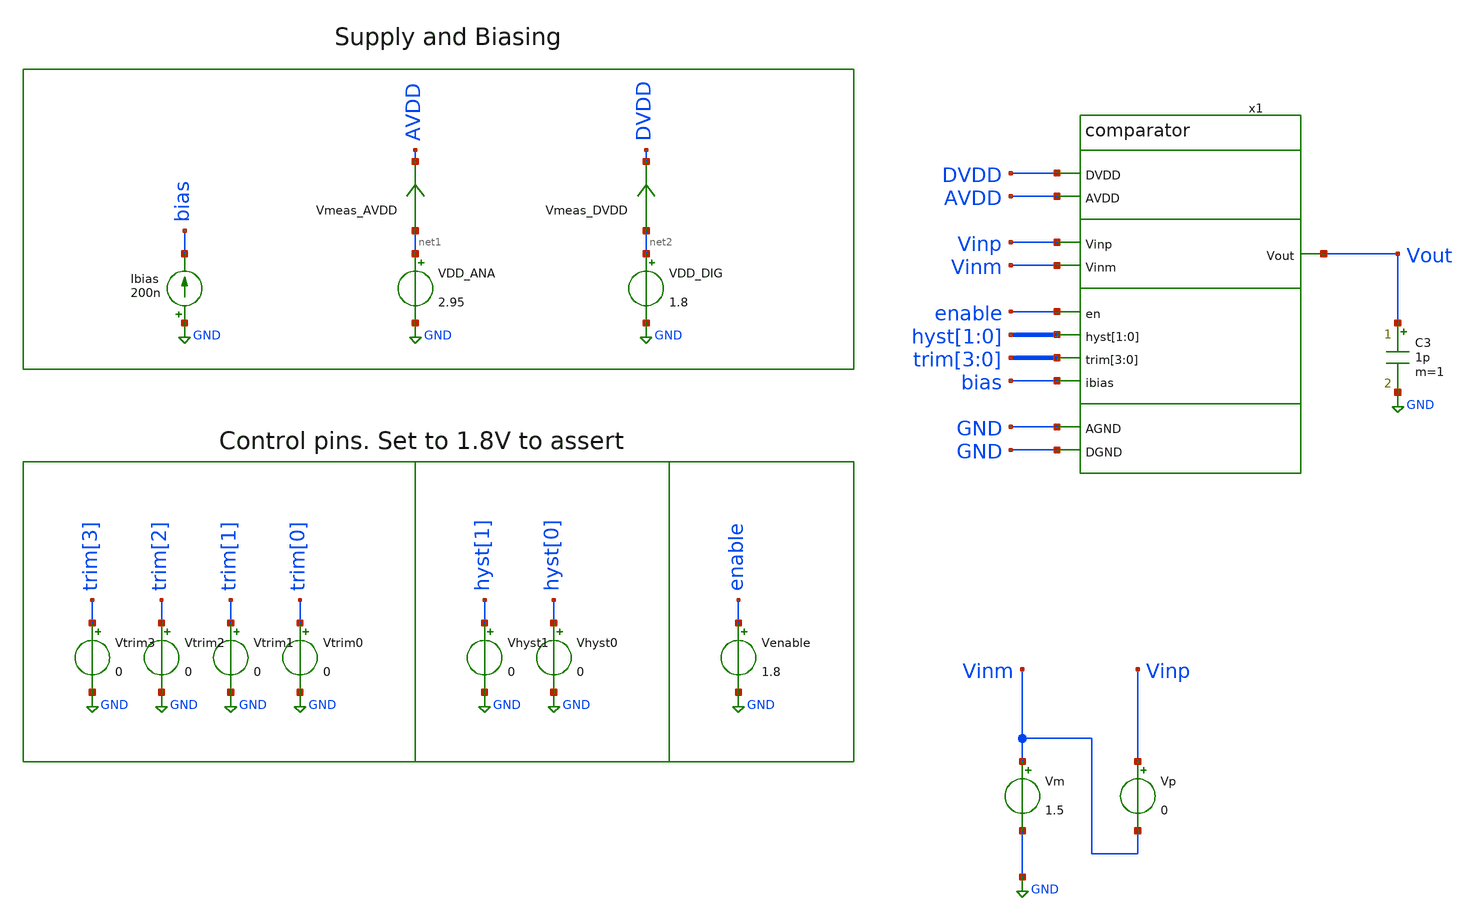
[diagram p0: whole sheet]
** sch_path: xschem/tb_comparator.sch
**.subckt tb_comparator
Vtrim3 trim[3] GND 0
Vp Vinp Vinm 0
VDD_ANA net1 GND 2.95
VDD_DIG net2 GND 1.8
Ibias GND bias 200n
C3 Vout GND 1p m=1
Vtrim2 trim[2] GND 0
Vtrim1 trim[1] GND 0
Vtrim0 trim[0] GND 0
Vm Vinm GND 1.5
Vhyst1 hyst[1] GND 0
Vhyst0 hyst[0] GND 0
x1 DVDD AVDD GND GND Vinp Vout Vinm enable hyst[1] hyst[0] trim[3] trim[2] trim[1] trim[0] bias
+ comparator
Venable enable GND 1.8
Vmeas_AVDD net1 AVDD 0
.save i(vmeas_avdd)
Vmeas_DVDD net2 DVDD 0
.save i(vmeas_dvdd)
**** begin user architecture code
.lib $::SKYWATER_MODELS/sky130.lib.spice tt



   *.dc Vp -10m 10m 0.05m Vm 0 5 0.25
   *.dc Vm 0 5 0.05 Vp -100m 100m 10m
   *.dc Vp 0 5 0.01
   .tran 100n 1m
.control
   *.tran 10n 13u 9u
   plot v(Vout)
   *plot v(Vinp)
   *plot v(Vinm)
   *plot v(x1.cmfb)
   *plot v(x1.vop)
   *plot v(x1.vom)
   *plot (v(x1.vop)+v(x1.vom))/2
   *plot v(x1.vop)-v(x1.vom)
   *plot v(x1.vdiff)
   meas tran current_avdd avg i(vmeas_avdd) from=500u to=1m
   meas tran current_dvdd avg i(vmeas_dvdd) from=500u to=1m
   wrdata test.txt current_avdd
.endc
.save all


**** end user architecture code
**.ends

* expanding   symbol:  comparator.sym # of pins=11
** sym_path: xschem/comparator.sym
** sch_path: xschem/comparator.sch
.subckt comparator DVDD AVDD AGND DGND Vinp Vout Vinm en hyst[1] hyst[0] trim[3] trim[2] trim[1]
+ trim[0] ibias
*.ipin Vinp
*.ipin Vinm
*.ipin AVDD
*.ipin AGND
*.ipin en
*.ipin hyst[1],hyst[0]
*.ipin trim[3],trim[2],trim[1],trim[0]
*.opin Vout
*.ipin DVDD
*.ipin ibias
*.ipin DGND
XM7 bias_n bias_n AGND AGND sky130_fd_pr__nfet_g5v0d10v5 L=1 W=2 nf=1 ad='int((nf+1)/2) * W/nf * 0.29'
+ as='int((nf+2)/2) * W/nf * 0.29' pd='2*int((nf+1)/2) * (W/nf + 0.29)' ps='2*int((nf+2)/2) * (W/nf + 0.29)'
+ nrd='0.29 / W' nrs='0.29 / W' sa=0 sb=0 sd=0 mult=2 m=2
XM6 stg1m_bot Vinm Vxm AGND sky130_fd_pr__nfet_g5v0d10v5 L=1 W=2 nf=1 ad='int((nf+1)/2) * W/nf * 0.29'
+ as='int((nf+2)/2) * W/nf * 0.29' pd='2*int((nf+1)/2) * (W/nf + 0.29)' ps='2*int((nf+2)/2) * (W/nf + 0.29)'
+ nrd='0.29 / W' nrs='0.29 / W' sa=0 sb=0 sd=0 mult=10 m=10
XM2 net1 bias_n AGND AGND sky130_fd_pr__nfet_g5v0d10v5 L=1 W=2 nf=1 ad='int((nf+1)/2) * W/nf * 0.29'
+ as='int((nf+2)/2) * W/nf * 0.29' pd='2*int((nf+1)/2) * (W/nf + 0.29)' ps='2*int((nf+2)/2) * (W/nf + 0.29)'
+ nrd='0.29 / W' nrs='0.29 / W' sa=0 sb=0 sd=0 mult=4 m=4
XM1 stg1p_bot Vinp Vxm AGND sky130_fd_pr__nfet_g5v0d10v5 L=1 W=2 nf=1 ad='int((nf+1)/2) * W/nf * 0.29'
+ as='int((nf+2)/2) * W/nf * 0.29' pd='2*int((nf+1)/2) * (W/nf + 0.29)' ps='2*int((nf+2)/2) * (W/nf + 0.29)'
+ nrd='0.29 / W' nrs='0.29 / W' sa=0 sb=0 sd=0 mult=10 m=10
XM3 stg1m_top stg1m_top AGND AGND sky130_fd_pr__nfet_g5v0d10v5 L=1 W=2 nf=1 ad='int((nf+1)/2) * W/nf * 0.29'
+ as='int((nf+2)/2) * W/nf * 0.29' pd='2*int((nf+1)/2) * (W/nf + 0.29)' ps='2*int((nf+2)/2) * (W/nf + 0.29)'
+ nrd='0.29 / W' nrs='0.29 / W' sa=0 sb=0 sd=0 mult=2 m=2
XM4 net7 bias_var AVDD AVDD sky130_fd_pr__pfet_g5v0d10v5 L=1 W=4 nf=2 ad='int((nf+1)/2) * W/nf * 0.29'
+ as='int((nf+2)/2) * W/nf * 0.29' pd='2*int((nf+1)/2) * (W/nf + 0.29)' ps='2*int((nf+2)/2) * (W/nf + 0.29)'
+ nrd='0.29 / W' nrs='0.29 / W' sa=0 sb=0 sd=0 mult=4 m=4
XM5 stg1m_top Vinm Vxp AVDD sky130_fd_pr__pfet_g5v0d10v5 L=1 W=4 nf=2 ad='int((nf+1)/2) * W/nf * 0.29'
+ as='int((nf+2)/2) * W/nf * 0.29' pd='2*int((nf+1)/2) * (W/nf + 0.29)' ps='2*int((nf+2)/2) * (W/nf + 0.29)'
+ nrd='0.29 / W' nrs='0.29 / W' sa=0 sb=0 sd=0 mult=10 m=10
XM17 stg1p_top Vinp Vxp AVDD sky130_fd_pr__pfet_g5v0d10v5 L=1 W=4 nf=2 ad='int((nf+1)/2) * W/nf * 0.29'
+ as='int((nf+2)/2) * W/nf * 0.29' pd='2*int((nf+1)/2) * (W/nf + 0.29)' ps='2*int((nf+2)/2) * (W/nf + 0.29)'
+ nrd='0.29 / W' nrs='0.29 / W' sa=0 sb=0 sd=0 mult=10 m=10
XM13 stg1m_bot stg1m_bot AVDD AVDD sky130_fd_pr__pfet_g5v0d10v5 L=1 W=4 nf=2 ad='int((nf+1)/2) * W/nf * 0.29'
+ as='int((nf+2)/2) * W/nf * 0.29' pd='2*int((nf+1)/2) * (W/nf + 0.29)' ps='2*int((nf+2)/2) * (W/nf + 0.29)'
+ nrd='0.29 / W' nrs='0.29 / W' sa=0 sb=0 sd=0 mult=2 m=2
XM9 Vop stg1m_bot AVDD AVDD sky130_fd_pr__pfet_g5v0d10v5 L=1 W=4 nf=2 ad='int((nf+1)/2) * W/nf * 0.29'
+ as='int((nf+2)/2) * W/nf * 0.29' pd='2*int((nf+1)/2) * (W/nf + 0.29)' ps='2*int((nf+2)/2) * (W/nf + 0.29)'
+ nrd='0.29 / W' nrs='0.29 / W' sa=0 sb=0 sd=0 mult=4 m=4
XM10 Vop stg1m_top AGND AGND sky130_fd_pr__nfet_g5v0d10v5 L=1 W=2 nf=1 ad='int((nf+1)/2) * W/nf * 0.29'
+ as='int((nf+2)/2) * W/nf * 0.29' pd='2*int((nf+1)/2) * (W/nf + 0.29)' ps='2*int((nf+2)/2) * (W/nf + 0.29)'
+ nrd='0.29 / W' nrs='0.29 / W' sa=0 sb=0 sd=0 mult=4 m=4
XM8 Vom stg1p_top AGND AGND sky130_fd_pr__nfet_g5v0d10v5 L=1 W=2 nf=1 ad='int((nf+1)/2) * W/nf * 0.29'
+ as='int((nf+2)/2) * W/nf * 0.29' pd='2*int((nf+1)/2) * (W/nf + 0.29)' ps='2*int((nf+2)/2) * (W/nf + 0.29)'
+ nrd='0.29 / W' nrs='0.29 / W' sa=0 sb=0 sd=0 mult=4 m=4
XM11 stg1p_top stg1p_top AGND AGND sky130_fd_pr__nfet_g5v0d10v5 L=1 W=2 nf=1 ad='int((nf+1)/2) * W/nf * 0.29'
+ as='int((nf+2)/2) * W/nf * 0.29' pd='2*int((nf+1)/2) * (W/nf + 0.29)' ps='2*int((nf+2)/2) * (W/nf + 0.29)'
+ nrd='0.29 / W' nrs='0.29 / W' sa=0 sb=0 sd=0 mult=2 m=2
XM12 Vom stg1p_bot AVDD AVDD sky130_fd_pr__pfet_g5v0d10v5 L=1 W=4 nf=2 ad='int((nf+1)/2) * W/nf * 0.29'
+ as='int((nf+2)/2) * W/nf * 0.29' pd='2*int((nf+1)/2) * (W/nf + 0.29)' ps='2*int((nf+2)/2) * (W/nf + 0.29)'
+ nrd='0.29 / W' nrs='0.29 / W' sa=0 sb=0 sd=0 mult=4 m=4
XM14 stg1p_bot stg1p_bot AVDD AVDD sky130_fd_pr__pfet_g5v0d10v5 L=1 W=4 nf=2 ad='int((nf+1)/2) * W/nf * 0.29'
+ as='int((nf+2)/2) * W/nf * 0.29' pd='2*int((nf+1)/2) * (W/nf + 0.29)' ps='2*int((nf+2)/2) * (W/nf + 0.29)'
+ nrd='0.29 / W' nrs='0.29 / W' sa=0 sb=0 sd=0 mult=2 m=2
XM18 Vom cmfb AGND AGND sky130_fd_pr__nfet_g5v0d10v5 L=1 W=2 nf=1 ad='int((nf+1)/2) * W/nf * 0.29' as='int((nf+2)/2) * W/nf * 0.29'
+ pd='2*int((nf+1)/2) * (W/nf + 0.29)' ps='2*int((nf+2)/2) * (W/nf + 0.29)' nrd='0.29 / W' nrs='0.29 / W'
+ sa=0 sb=0 sd=0 mult=4 m=4
XM19 Vop cmfb AGND AGND sky130_fd_pr__nfet_g5v0d10v5 L=1 W=2 nf=1 ad='int((nf+1)/2) * W/nf * 0.29' as='int((nf+2)/2) * W/nf * 0.29'
+ pd='2*int((nf+1)/2) * (W/nf + 0.29)' ps='2*int((nf+2)/2) * (W/nf + 0.29)' nrd='0.29 / W' nrs='0.29 / W'
+ sa=0 sb=0 sd=0 mult=4 m=4
XM20 Vom bias_var AVDD AVDD sky130_fd_pr__pfet_g5v0d10v5 L=1 W=4 nf=2 ad='int((nf+1)/2) * W/nf * 0.29'
+ as='int((nf+2)/2) * W/nf * 0.29' pd='2*int((nf+1)/2) * (W/nf + 0.29)' ps='2*int((nf+2)/2) * (W/nf + 0.29)'
+ nrd='0.29 / W' nrs='0.29 / W' sa=0 sb=0 sd=0 mult=6 m=6
XM21 Vop bias_var AVDD AVDD sky130_fd_pr__pfet_g5v0d10v5 L=1 W=4 nf=2 ad='int((nf+1)/2) * W/nf * 0.29'
+ as='int((nf+2)/2) * W/nf * 0.29' pd='2*int((nf+1)/2) * (W/nf + 0.29)' ps='2*int((nf+2)/2) * (W/nf + 0.29)'
+ nrd='0.29 / W' nrs='0.29 / W' sa=0 sb=0 sd=0 mult=6 m=6
XM22 net2 bias_p AVDD AVDD sky130_fd_pr__pfet_g5v0d10v5 L=1 W=4 nf=2 ad='int((nf+1)/2) * W/nf * 0.29'
+ as='int((nf+2)/2) * W/nf * 0.29' pd='2*int((nf+1)/2) * (W/nf + 0.29)' ps='2*int((nf+2)/2) * (W/nf + 0.29)'
+ nrd='0.29 / W' nrs='0.29 / W' sa=0 sb=0 sd=0 mult=2 m=2
XM23 Vom_stg2 Vom net2 AVDD sky130_fd_pr__pfet_g5v0d10v5 L=1 W=4 nf=2 ad='int((nf+1)/2) * W/nf * 0.29'
+ as='int((nf+2)/2) * W/nf * 0.29' pd='2*int((nf+1)/2) * (W/nf + 0.29)' ps='2*int((nf+2)/2) * (W/nf + 0.29)'
+ nrd='0.29 / W' nrs='0.29 / W' sa=0 sb=0 sd=0 mult=2 m=2
XM24 Vop_stg2 Vop net2 AVDD sky130_fd_pr__pfet_g5v0d10v5 L=1 W=4 nf=2 ad='int((nf+1)/2) * W/nf * 0.29'
+ as='int((nf+2)/2) * W/nf * 0.29' pd='2*int((nf+1)/2) * (W/nf + 0.29)' ps='2*int((nf+2)/2) * (W/nf + 0.29)'
+ nrd='0.29 / W' nrs='0.29 / W' sa=0 sb=0 sd=0 mult=2 m=2
XM25 Vop_stg2 Vop_stg2 DGND DGND sky130_fd_pr__nfet_g5v0d10v5 L=1 W=2 nf=1 ad='int((nf+1)/2) * W/nf * 0.29'
+ as='int((nf+2)/2) * W/nf * 0.29' pd='2*int((nf+1)/2) * (W/nf + 0.29)' ps='2*int((nf+2)/2) * (W/nf + 0.29)'
+ nrd='0.29 / W' nrs='0.29 / W' sa=0 sb=0 sd=0 mult=2 m=2
XM26 Vom_stg2 Vom_stg2 DGND DGND sky130_fd_pr__nfet_g5v0d10v5 L=1 W=2 nf=1 ad='int((nf+1)/2) * W/nf * 0.29'
+ as='int((nf+2)/2) * W/nf * 0.29' pd='2*int((nf+1)/2) * (W/nf + 0.29)' ps='2*int((nf+2)/2) * (W/nf + 0.29)'
+ nrd='0.29 / W' nrs='0.29 / W' sa=0 sb=0 sd=0 mult=2 m=2
XM27 net3 Vom_stg2 DGND DGND sky130_fd_pr__nfet_g5v0d10v5 L=1 W=2 nf=1 ad='int((nf+1)/2) * W/nf * 0.29'
+ as='int((nf+2)/2) * W/nf * 0.29' pd='2*int((nf+1)/2) * (W/nf + 0.29)' ps='2*int((nf+2)/2) * (W/nf + 0.29)'
+ nrd='0.29 / W' nrs='0.29 / W' sa=0 sb=0 sd=0 mult=2 m=2
XM28 Vdiff Vop_stg2 DGND DGND sky130_fd_pr__nfet_g5v0d10v5 L=1 W=2 nf=1 ad='int((nf+1)/2) * W/nf * 0.29'
+ as='int((nf+2)/2) * W/nf * 0.29' pd='2*int((nf+1)/2) * (W/nf + 0.29)' ps='2*int((nf+2)/2) * (W/nf + 0.29)'
+ nrd='0.29 / W' nrs='0.29 / W' sa=0 sb=0 sd=0 mult=2 m=2
XM29 Vdiff net3 DVDD DVDD sky130_fd_pr__pfet_01v8 L=1 W=4 nf=1 ad='int((nf+1)/2) * W/nf * 0.29' as='int((nf+2)/2) * W/nf * 0.29'
+ pd='2*int((nf+1)/2) * (W/nf + 0.29)' ps='2*int((nf+2)/2) * (W/nf + 0.29)' nrd='0.29 / W' nrs='0.29 / W'
+ sa=0 sb=0 sd=0 mult=2 m=2
XM30 net3 net3 DVDD DVDD sky130_fd_pr__pfet_01v8 L=1 W=4 nf=1 ad='int((nf+1)/2) * W/nf * 0.29' as='int((nf+2)/2) * W/nf * 0.29'
+ pd='2*int((nf+1)/2) * (W/nf + 0.29)' ps='2*int((nf+2)/2) * (W/nf + 0.29)' nrd='0.29 / W' nrs='0.29 / W'
+ sa=0 sb=0 sd=0 mult=2 m=2
XM31 Vout Vdiff DVDD DVDD sky130_fd_pr__pfet_01v8 L=0.15 W=1 nf=2 ad='int((nf+1)/2) * W/nf * 0.29' as='int((nf+2)/2) * W/nf * 0.29'
+ pd='2*int((nf+1)/2) * (W/nf + 0.29)' ps='2*int((nf+2)/2) * (W/nf + 0.29)' nrd='0.29 / W' nrs='0.29 / W'
+ sa=0 sb=0 sd=0 mult=1 m=1
XM44 Vout Vdiff DGND DGND sky130_fd_pr__nfet_01v8 L=0.15 W=0.5 nf=1 ad='int((nf+1)/2) * W/nf * 0.29'
+ as='int((nf+2)/2) * W/nf * 0.29' pd='2*int((nf+1)/2) * (W/nf + 0.29)' ps='2*int((nf+2)/2) * (W/nf + 0.29)'
+ nrd='0.29 / W' nrs='0.29 / W' sa=0 sb=0 sd=0 mult=1 m=1
XM45 ibias ibias bias_n AGND sky130_fd_pr__nfet_g5v0d10v5 L=1 W=2 nf=1 ad='int((nf+1)/2) * W/nf * 0.29'
+ as='int((nf+2)/2) * W/nf * 0.29' pd='2*int((nf+1)/2) * (W/nf + 0.29)' ps='2*int((nf+2)/2) * (W/nf + 0.29)'
+ nrd='0.29 / W' nrs='0.29 / W' sa=0 sb=0 sd=0 mult=1 m=1
XM48 bias_n enb_hv AGND AGND sky130_fd_pr__nfet_g5v0d10v5 L=0.5 W=2 nf=1 ad='int((nf+1)/2) * W/nf * 0.29'
+ as='int((nf+2)/2) * W/nf * 0.29' pd='2*int((nf+1)/2) * (W/nf + 0.29)' ps='2*int((nf+2)/2) * (W/nf + 0.29)'
+ nrd='0.29 / W' nrs='0.29 / W' sa=0 sb=0 sd=0 mult=4 m=4
XM40 net4 bias_hyst net8 AGND sky130_fd_pr__nfet_g5v0d10v5 L=1 W=2 nf=1 ad='int((nf+1)/2) * W/nf * 0.29'
+ as='int((nf+2)/2) * W/nf * 0.29' pd='2*int((nf+1)/2) * (W/nf + 0.29)' ps='2*int((nf+2)/2) * (W/nf + 0.29)'
+ nrd='0.29 / W' nrs='0.29 / W' sa=0 sb=0 sd=0 mult=3 m=3
XM53 net11 Vout net4 AGND sky130_fd_pr__nfet_g5v0d10v5 L=1 W=2 nf=1 ad='int((nf+1)/2) * W/nf * 0.29'
+ as='int((nf+2)/2) * W/nf * 0.29' pd='2*int((nf+1)/2) * (W/nf + 0.29)' ps='2*int((nf+2)/2) * (W/nf + 0.29)'
+ nrd='0.29 / W' nrs='0.29 / W' sa=0 sb=0 sd=0 mult=1 m=1
XM54 net10 Voutb net4 AGND sky130_fd_pr__nfet_g5v0d10v5 L=1 W=2 nf=1 ad='int((nf+1)/2) * W/nf * 0.29'
+ as='int((nf+2)/2) * W/nf * 0.29' pd='2*int((nf+1)/2) * (W/nf + 0.29)' ps='2*int((nf+2)/2) * (W/nf + 0.29)'
+ nrd='0.29 / W' nrs='0.29 / W' sa=0 sb=0 sd=0 mult=1 m=1
XM61 net5 stg1p_bot AVDD AVDD sky130_fd_pr__pfet_g5v0d10v5 L=1 W=4 nf=2 ad='int((nf+1)/2) * W/nf * 0.29'
+ as='int((nf+2)/2) * W/nf * 0.29' pd='2*int((nf+1)/2) * (W/nf + 0.29)' ps='2*int((nf+2)/2) * (W/nf + 0.29)'
+ nrd='0.29 / W' nrs='0.29 / W' sa=0 sb=0 sd=0 mult=2 m=2
XM62 net5 stg1m_bot AVDD AVDD sky130_fd_pr__pfet_g5v0d10v5 L=1 W=4 nf=2 ad='int((nf+1)/2) * W/nf * 0.29'
+ as='int((nf+2)/2) * W/nf * 0.29' pd='2*int((nf+1)/2) * (W/nf + 0.29)' ps='2*int((nf+2)/2) * (W/nf + 0.29)'
+ nrd='0.29 / W' nrs='0.29 / W' sa=0 sb=0 sd=0 mult=2 m=2
XM70 net5 bias_n AGND AGND sky130_fd_pr__nfet_g5v0d10v5 L=1 W=2 nf=1 ad='int((nf+1)/2) * W/nf * 0.29'
+ as='int((nf+2)/2) * W/nf * 0.29' pd='2*int((nf+1)/2) * (W/nf + 0.29)' ps='2*int((nf+2)/2) * (W/nf + 0.29)'
+ nrd='0.29 / W' nrs='0.29 / W' sa=0 sb=0 sd=0 mult=4 m=4
XM72 bias_var bias_var AVDD AVDD sky130_fd_pr__pfet_g5v0d10v5 L=1 W=4 nf=2 ad='int((nf+1)/2) * W/nf * 0.29'
+ as='int((nf+2)/2) * W/nf * 0.29' pd='2*int((nf+1)/2) * (W/nf + 0.29)' ps='2*int((nf+2)/2) * (W/nf + 0.29)'
+ nrd='0.29 / W' nrs='0.29 / W' sa=0 sb=0 sd=0 mult=4 m=4
XM63 net5 net5 bias_var AVDD sky130_fd_pr__pfet_g5v0d10v5 L=1 W=4 nf=2 ad='int((nf+1)/2) * W/nf * 0.29'
+ as='int((nf+2)/2) * W/nf * 0.29' pd='2*int((nf+1)/2) * (W/nf + 0.29)' ps='2*int((nf+2)/2) * (W/nf + 0.29)'
+ nrd='0.29 / W' nrs='0.29 / W' sa=0 sb=0 sd=0 mult=4 m=4
XM64 Vom bias_p AVDD AVDD sky130_fd_pr__pfet_g5v0d10v5 L=1 W=4 nf=2 ad='int((nf+1)/2) * W/nf * 0.29'
+ as='int((nf+2)/2) * W/nf * 0.29' pd='2*int((nf+1)/2) * (W/nf + 0.29)' ps='2*int((nf+2)/2) * (W/nf + 0.29)'
+ nrd='0.29 / W' nrs='0.29 / W' sa=0 sb=0 sd=0 mult=2 m=2
XM71 Vop bias_p AVDD AVDD sky130_fd_pr__pfet_g5v0d10v5 L=1 W=4 nf=2 ad='int((nf+1)/2) * W/nf * 0.29'
+ as='int((nf+2)/2) * W/nf * 0.29' pd='2*int((nf+1)/2) * (W/nf + 0.29)' ps='2*int((nf+2)/2) * (W/nf + 0.29)'
+ nrd='0.29 / W' nrs='0.29 / W' sa=0 sb=0 sd=0 mult=2 m=2
XM73 net4 bias_hyst net9 AGND sky130_fd_pr__nfet_g5v0d10v5 L=1 W=2 nf=1 ad='int((nf+1)/2) * W/nf * 0.29'
+ as='int((nf+2)/2) * W/nf * 0.29' pd='2*int((nf+1)/2) * (W/nf + 0.29)' ps='2*int((nf+2)/2) * (W/nf + 0.29)'
+ nrd='0.29 / W' nrs='0.29 / W' sa=0 sb=0 sd=0 mult=1 m=1
XM75 Voutb Vout DVDD DVDD sky130_fd_pr__pfet_01v8 L=0.15 W=1 nf=2 ad='int((nf+1)/2) * W/nf * 0.29' as='int((nf+2)/2) * W/nf * 0.29'
+ pd='2*int((nf+1)/2) * (W/nf + 0.29)' ps='2*int((nf+2)/2) * (W/nf + 0.29)' nrd='0.29 / W' nrs='0.29 / W'
+ sa=0 sb=0 sd=0 mult=1 m=1
XM76 Voutb Vout DGND DGND sky130_fd_pr__nfet_01v8 L=0.15 W=0.5 nf=1 ad='int((nf+1)/2) * W/nf * 0.29'
+ as='int((nf+2)/2) * W/nf * 0.29' pd='2*int((nf+1)/2) * (W/nf + 0.29)' ps='2*int((nf+2)/2) * (W/nf + 0.29)'
+ nrd='0.29 / W' nrs='0.29 / W' sa=0 sb=0 sd=0 mult=1 m=1
XM77 bias_p2 bias_p AVDD AVDD sky130_fd_pr__pfet_g5v0d10v5 L=1 W=4 nf=2 ad='int((nf+1)/2) * W/nf * 0.29'
+ as='int((nf+2)/2) * W/nf * 0.29' pd='2*int((nf+1)/2) * (W/nf + 0.29)' ps='2*int((nf+2)/2) * (W/nf + 0.29)'
+ nrd='0.29 / W' nrs='0.29 / W' sa=0 sb=0 sd=0 mult=2 m=2
XM78 bias_hyst bias_hyst AGND AGND sky130_fd_pr__nfet_g5v0d10v5 L=1 W=2 nf=1 ad='int((nf+1)/2) * W/nf * 0.29'
+ as='int((nf+2)/2) * W/nf * 0.29' pd='2*int((nf+1)/2) * (W/nf + 0.29)' ps='2*int((nf+2)/2) * (W/nf + 0.29)'
+ nrd='0.29 / W' nrs='0.29 / W' sa=0 sb=0 sd=0 mult=6 m=6
XM79 bias_hyst net6 bias_p2 AVDD sky130_fd_pr__pfet_g5v0d10v5 L=1 W=4 nf=2 ad='int((nf+1)/2) * W/nf * 0.29'
+ as='int((nf+2)/2) * W/nf * 0.29' pd='2*int((nf+1)/2) * (W/nf + 0.29)' ps='2*int((nf+2)/2) * (W/nf + 0.29)'
+ nrd='0.29 / W' nrs='0.29 / W' sa=0 sb=0 sd=0 mult=8 m=8
XM90 Vxm ibias net1 AGND sky130_fd_pr__nfet_g5v0d10v5 L=1 W=2 nf=1 ad='int((nf+1)/2) * W/nf * 0.29' as='int((nf+2)/2) * W/nf * 0.29'
+ pd='2*int((nf+1)/2) * (W/nf + 0.29)' ps='2*int((nf+2)/2) * (W/nf + 0.29)' nrd='0.29 / W' nrs='0.29 / W'
+ sa=0 sb=0 sd=0 mult=4 m=4
XM91 Vxp bias_p2 net7 AVDD sky130_fd_pr__pfet_g5v0d10v5 L=1 W=4 nf=2 ad='int((nf+1)/2) * W/nf * 0.29'
+ as='int((nf+2)/2) * W/nf * 0.29' pd='2*int((nf+1)/2) * (W/nf + 0.29)' ps='2*int((nf+2)/2) * (W/nf + 0.29)'
+ nrd='0.29 / W' nrs='0.29 / W' sa=0 sb=0 sd=0 mult=4 m=4
XM94 net6 bias_n AGND AGND sky130_fd_pr__nfet_g5v0d10v5 L=1 W=2 nf=1 ad='int((nf+1)/2) * W/nf * 0.29'
+ as='int((nf+2)/2) * W/nf * 0.29' pd='2*int((nf+1)/2) * (W/nf + 0.29)' ps='2*int((nf+2)/2) * (W/nf + 0.29)'
+ nrd='0.29 / W' nrs='0.29 / W' sa=0 sb=0 sd=0 mult=2 m=2
XM95 bias_p bias_p AVDD AVDD sky130_fd_pr__pfet_g5v0d10v5 L=1 W=4 nf=2 ad='int((nf+1)/2) * W/nf * 0.29'
+ as='int((nf+2)/2) * W/nf * 0.29' pd='2*int((nf+1)/2) * (W/nf + 0.29)' ps='2*int((nf+2)/2) * (W/nf + 0.29)'
+ nrd='0.29 / W' nrs='0.29 / W' sa=0 sb=0 sd=0 mult=2 m=2
XM96 net6 net6 bias_p AVDD sky130_fd_pr__pfet_g5v0d10v5 L=1 W=4 nf=2 ad='int((nf+1)/2) * W/nf * 0.29'
+ as='int((nf+2)/2) * W/nf * 0.29' pd='2*int((nf+1)/2) * (W/nf + 0.29)' ps='2*int((nf+2)/2) * (W/nf + 0.29)'
+ nrd='0.29 / W' nrs='0.29 / W' sa=0 sb=0 sd=0 mult=1 m=1
XM16 net8 hyst1_hv AGND AGND sky130_fd_pr__nfet_g5v0d10v5 L=0.5 W=2 nf=1 ad='int((nf+1)/2) * W/nf * 0.29'
+ as='int((nf+2)/2) * W/nf * 0.29' pd='2*int((nf+1)/2) * (W/nf + 0.29)' ps='2*int((nf+2)/2) * (W/nf + 0.29)'
+ nrd='0.29 / W' nrs='0.29 / W' sa=0 sb=0 sd=0 mult=6 m=6
XM33 net9 hyst0_hv AGND AGND sky130_fd_pr__nfet_g5v0d10v5 L=0.5 W=2 nf=1 ad='int((nf+1)/2) * W/nf * 0.29'
+ as='int((nf+2)/2) * W/nf * 0.29' pd='2*int((nf+1)/2) * (W/nf + 0.29)' ps='2*int((nf+2)/2) * (W/nf + 0.29)'
+ nrd='0.29 / W' nrs='0.29 / W' sa=0 sb=0 sd=0 mult=2 m=2
XM35 net10 net10 AVDD AVDD sky130_fd_pr__pfet_g5v0d10v5 L=1 W=4 nf=2 ad='int((nf+1)/2) * W/nf * 0.29'
+ as='int((nf+2)/2) * W/nf * 0.29' pd='2*int((nf+1)/2) * (W/nf + 0.29)' ps='2*int((nf+2)/2) * (W/nf + 0.29)'
+ nrd='0.29 / W' nrs='0.29 / W' sa=0 sb=0 sd=0 mult=2 m=2
XM37 stg1m_top net10 AVDD AVDD sky130_fd_pr__pfet_g5v0d10v5 L=1 W=4 nf=2 ad='int((nf+1)/2) * W/nf * 0.29'
+ as='int((nf+2)/2) * W/nf * 0.29' pd='2*int((nf+1)/2) * (W/nf + 0.29)' ps='2*int((nf+2)/2) * (W/nf + 0.29)'
+ nrd='0.29 / W' nrs='0.29 / W' sa=0 sb=0 sd=0 mult=2 m=2
XM41 stg1p_top net11 AVDD AVDD sky130_fd_pr__pfet_g5v0d10v5 L=1 W=4 nf=2 ad='int((nf+1)/2) * W/nf * 0.29'
+ as='int((nf+2)/2) * W/nf * 0.29' pd='2*int((nf+1)/2) * (W/nf + 0.29)' ps='2*int((nf+2)/2) * (W/nf + 0.29)'
+ nrd='0.29 / W' nrs='0.29 / W' sa=0 sb=0 sd=0 mult=2 m=2
XM42 net11 net11 AVDD AVDD sky130_fd_pr__pfet_g5v0d10v5 L=1 W=4 nf=2 ad='int((nf+1)/2) * W/nf * 0.29'
+ as='int((nf+2)/2) * W/nf * 0.29' pd='2*int((nf+1)/2) * (W/nf + 0.29)' ps='2*int((nf+2)/2) * (W/nf + 0.29)'
+ nrd='0.29 / W' nrs='0.29 / W' sa=0 sb=0 sd=0 mult=2 m=2
XM43 net12 bias_trim net13 AGND sky130_fd_pr__nfet_g5v0d10v5 L=1 W=2 nf=1 ad='int((nf+1)/2) * W/nf * 0.29'
+ as='int((nf+2)/2) * W/nf * 0.29' pd='2*int((nf+1)/2) * (W/nf + 0.29)' ps='2*int((nf+2)/2) * (W/nf + 0.29)'
+ nrd='0.29 / W' nrs='0.29 / W' sa=0 sb=0 sd=0 mult=4 m=4
XM46 net11 trim3_lv net12 AGND sky130_fd_pr__nfet_g5v0d10v5 L=1 W=2 nf=1 ad='int((nf+1)/2) * W/nf * 0.29'
+ as='int((nf+2)/2) * W/nf * 0.29' pd='2*int((nf+1)/2) * (W/nf + 0.29)' ps='2*int((nf+2)/2) * (W/nf + 0.29)'
+ nrd='0.29 / W' nrs='0.29 / W' sa=0 sb=0 sd=0 mult=1 m=1
XM47 net10 trim3b_lv net12 AGND sky130_fd_pr__nfet_g5v0d10v5 L=1 W=2 nf=1 ad='int((nf+1)/2) * W/nf * 0.29'
+ as='int((nf+2)/2) * W/nf * 0.29' pd='2*int((nf+1)/2) * (W/nf + 0.29)' ps='2*int((nf+2)/2) * (W/nf + 0.29)'
+ nrd='0.29 / W' nrs='0.29 / W' sa=0 sb=0 sd=0 mult=1 m=1
XM50 net12 bias_trim net14 AGND sky130_fd_pr__nfet_g5v0d10v5 L=1 W=2 nf=1 ad='int((nf+1)/2) * W/nf * 0.29'
+ as='int((nf+2)/2) * W/nf * 0.29' pd='2*int((nf+1)/2) * (W/nf + 0.29)' ps='2*int((nf+2)/2) * (W/nf + 0.29)'
+ nrd='0.29 / W' nrs='0.29 / W' sa=0 sb=0 sd=0 mult=2 m=2
XM51 net13 trim2_hv AGND AGND sky130_fd_pr__nfet_g5v0d10v5 L=0.5 W=2 nf=1 ad='int((nf+1)/2) * W/nf * 0.29'
+ as='int((nf+2)/2) * W/nf * 0.29' pd='2*int((nf+1)/2) * (W/nf + 0.29)' ps='2*int((nf+2)/2) * (W/nf + 0.29)'
+ nrd='0.29 / W' nrs='0.29 / W' sa=0 sb=0 sd=0 mult=8 m=8
XM52 net14 trim1_hv AGND AGND sky130_fd_pr__nfet_g5v0d10v5 L=0.5 W=2 nf=1 ad='int((nf+1)/2) * W/nf * 0.29'
+ as='int((nf+2)/2) * W/nf * 0.29' pd='2*int((nf+1)/2) * (W/nf + 0.29)' ps='2*int((nf+2)/2) * (W/nf + 0.29)'
+ nrd='0.29 / W' nrs='0.29 / W' sa=0 sb=0 sd=0 mult=4 m=4
XM55 net12 bias_trim net15 AGND sky130_fd_pr__nfet_g5v0d10v5 L=1 W=2 nf=1 ad='int((nf+1)/2) * W/nf * 0.29'
+ as='int((nf+2)/2) * W/nf * 0.29' pd='2*int((nf+1)/2) * (W/nf + 0.29)' ps='2*int((nf+2)/2) * (W/nf + 0.29)'
+ nrd='0.29 / W' nrs='0.29 / W' sa=0 sb=0 sd=0 mult=1 m=1
XM56 net15 trim0_hv AGND AGND sky130_fd_pr__nfet_g5v0d10v5 L=0.5 W=2 nf=1 ad='int((nf+1)/2) * W/nf * 0.29'
+ as='int((nf+2)/2) * W/nf * 0.29' pd='2*int((nf+1)/2) * (W/nf + 0.29)' ps='2*int((nf+2)/2) * (W/nf + 0.29)'
+ nrd='0.29 / W' nrs='0.29 / W' sa=0 sb=0 sd=0 mult=2 m=2
XM57 net16 bias_p AVDD AVDD sky130_fd_pr__pfet_g5v0d10v5 L=1 W=4 nf=2 ad='int((nf+1)/2) * W/nf * 0.29'
+ as='int((nf+2)/2) * W/nf * 0.29' pd='2*int((nf+1)/2) * (W/nf + 0.29)' ps='2*int((nf+2)/2) * (W/nf + 0.29)'
+ nrd='0.29 / W' nrs='0.29 / W' sa=0 sb=0 sd=0 mult=1 m=1
XM58 bias_trim bias_trim AGND AGND sky130_fd_pr__nfet_g5v0d10v5 L=1 W=4 nf=1 ad='int((nf+1)/2) * W/nf * 0.29'
+ as='int((nf+2)/2) * W/nf * 0.29' pd='2*int((nf+1)/2) * (W/nf + 0.29)' ps='2*int((nf+2)/2) * (W/nf + 0.29)'
+ nrd='0.29 / W' nrs='0.29 / W' sa=0 sb=0 sd=0 mult=18 m=18
XM59 bias_trim net6 net16 AVDD sky130_fd_pr__pfet_g5v0d10v5 L=1 W=4 nf=2 ad='int((nf+1)/2) * W/nf * 0.29'
+ as='int((nf+2)/2) * W/nf * 0.29' pd='2*int((nf+1)/2) * (W/nf + 0.29)' ps='2*int((nf+2)/2) * (W/nf + 0.29)'
+ nrd='0.29 / W' nrs='0.29 / W' sa=0 sb=0 sd=0 mult=4 m=4
XM65 Vcm Vcm AVDD AVDD sky130_fd_pr__pfet_g5v0d10v5 L=8 W=2 nf=1 ad='int((nf+1)/2) * W/nf * 0.29' as='int((nf+2)/2) * W/nf * 0.29'
+ pd='2*int((nf+1)/2) * (W/nf + 0.29)' ps='2*int((nf+2)/2) * (W/nf + 0.29)' nrd='0.29 / W' nrs='0.29 / W'
+ sa=0 sb=0 sd=0 mult=1 m=1
XM66 Vcm Vcm AGND AGND sky130_fd_pr__nfet_g5v0d10v5 L=8 W=2 nf=1 ad='int((nf+1)/2) * W/nf * 0.29' as='int((nf+2)/2) * W/nf * 0.29'
+ pd='2*int((nf+1)/2) * (W/nf + 0.29)' ps='2*int((nf+2)/2) * (W/nf + 0.29)' nrd='0.29 / W' nrs='0.29 / W'
+ sa=0 sb=0 sd=0 mult=1 m=1
XM67 Vop_stg2 Vom_stg2 DGND DGND sky130_fd_pr__nfet_g5v0d10v5 L=0.5 W=1 nf=1 ad='int((nf+1)/2) * W/nf * 0.29'
+ as='int((nf+2)/2) * W/nf * 0.29' pd='2*int((nf+1)/2) * (W/nf + 0.29)' ps='2*int((nf+2)/2) * (W/nf + 0.29)'
+ nrd='0.29 / W' nrs='0.29 / W' sa=0 sb=0 sd=0 mult=1 m=1
XM69 Vom_stg2 Vop_stg2 DGND DGND sky130_fd_pr__nfet_g5v0d10v5 L=0.5 W=1 nf=1 ad='int((nf+1)/2) * W/nf * 0.29'
+ as='int((nf+2)/2) * W/nf * 0.29' pd='2*int((nf+1)/2) * (W/nf + 0.29)' ps='2*int((nf+2)/2) * (W/nf + 0.29)'
+ nrd='0.29 / W' nrs='0.29 / W' sa=0 sb=0 sd=0 mult=1 m=1
XM15 bias_p en_hv AVDD AVDD sky130_fd_pr__pfet_g5v0d10v5 L=0.5 W=4 nf=2 ad='int((nf+1)/2) * W/nf * 0.29'
+ as='int((nf+2)/2) * W/nf * 0.29' pd='2*int((nf+1)/2) * (W/nf + 0.29)' ps='2*int((nf+2)/2) * (W/nf + 0.29)'
+ nrd='0.29 / W' nrs='0.29 / W' sa=0 sb=0 sd=0 mult=4 m=4
x9 AVDD AGND Vop cmfb Vom Vcm bias_p cmfb
x2 AVDD DVDD DGND trim2b_hv trim2_hv trim[2] AGND level_shifter_up
x1 DVDD trim3_lv trim3b_lv DGND inverter
x3 DVDD trim3b_lv trim[3] DGND inverter
x4 AVDD DVDD DGND trim1b_hv trim1_hv trim[1] AGND level_shifter_up
x5 AVDD DVDD DGND trim0b_hv trim0_hv trim[0] AGND level_shifter_up
x6 AVDD DVDD DGND enb_hv en_hv en AGND level_shifter_up
x7 AVDD DVDD DGND hyst1b_hv hyst1_hv hyst[1] AGND level_shifter_up
x8 AVDD DVDD DGND hyst0b_hv hyst0_hv hyst[0] AGND level_shifter_up
.ends


* expanding   symbol:  sky130_ak_ip__comparator/xschem/cmfb.sym # of pins=7
** sym_path: xschem/cmfb.sym
** sch_path: xschem/cmfb.sch
.subckt cmfb VDD GND Vp Vcmfb Vm Vcm bias_p
*.ipin Vp
*.ipin Vm
*.ipin VDD
*.opin Vcmfb
*.ipin GND
*.ipin Vcm
*.ipin bias_p
XM32 net1 bias_p VDD VDD sky130_fd_pr__pfet_g5v0d10v5 L=4 W=4 nf=2 ad='int((nf+1)/2) * W/nf * 0.29' as='int((nf+2)/2) * W/nf * 0.29'
+ pd='2*int((nf+1)/2) * (W/nf + 0.29)' ps='2*int((nf+2)/2) * (W/nf + 0.29)' nrd='0.29 / W' nrs='0.29 / W'
+ sa=0 sb=0 sd=0 mult=1 m=1
XM34 net2 Vm net1 VDD sky130_fd_pr__pfet_g5v0d10v5 L=0.5 W=4 nf=2 ad='int((nf+1)/2) * W/nf * 0.29' as='int((nf+2)/2) * W/nf * 0.29'
+ pd='2*int((nf+1)/2) * (W/nf + 0.29)' ps='2*int((nf+2)/2) * (W/nf + 0.29)' nrd='0.29 / W' nrs='0.29 / W'
+ sa=0 sb=0 sd=0 mult=1 m=1
XM36 Vcmfb Vcm net1 VDD sky130_fd_pr__pfet_g5v0d10v5 L=0.5 W=4 nf=2 ad='int((nf+1)/2) * W/nf * 0.29'
+ as='int((nf+2)/2) * W/nf * 0.29' pd='2*int((nf+1)/2) * (W/nf + 0.29)' ps='2*int((nf+2)/2) * (W/nf + 0.29)'
+ nrd='0.29 / W' nrs='0.29 / W' sa=0 sb=0 sd=0 mult=1 m=1
XM38 Vcmfb net2 GND GND sky130_fd_pr__nfet_g5v0d10v5 L=0.5 W=4 nf=1 ad='int((nf+1)/2) * W/nf * 0.29'
+ as='int((nf+2)/2) * W/nf * 0.29' pd='2*int((nf+1)/2) * (W/nf + 0.29)' ps='2*int((nf+2)/2) * (W/nf + 0.29)'
+ nrd='0.29 / W' nrs='0.29 / W' sa=0 sb=0 sd=0 mult=2 m=2
XM39 net2 net2 GND GND sky130_fd_pr__nfet_g5v0d10v5 L=0.5 W=4 nf=1 ad='int((nf+1)/2) * W/nf * 0.29' as='int((nf+2)/2) * W/nf * 0.29'
+ pd='2*int((nf+1)/2) * (W/nf + 0.29)' ps='2*int((nf+2)/2) * (W/nf + 0.29)' nrd='0.29 / W' nrs='0.29 / W'
+ sa=0 sb=0 sd=0 mult=2 m=2
C3 Vcmfb GND 20p m=1
XM15 Vcmfb Vcm net3 VDD sky130_fd_pr__pfet_g5v0d10v5 L=0.5 W=4 nf=2 ad='int((nf+1)/2) * W/nf * 0.29'
+ as='int((nf+2)/2) * W/nf * 0.29' pd='2*int((nf+1)/2) * (W/nf + 0.29)' ps='2*int((nf+2)/2) * (W/nf + 0.29)'
+ nrd='0.29 / W' nrs='0.29 / W' sa=0 sb=0 sd=0 mult=1 m=1
XM49 net3 bias_p VDD VDD sky130_fd_pr__pfet_g5v0d10v5 L=4 W=4 nf=2 ad='int((nf+1)/2) * W/nf * 0.29' as='int((nf+2)/2) * W/nf * 0.29'
+ pd='2*int((nf+1)/2) * (W/nf + 0.29)' ps='2*int((nf+2)/2) * (W/nf + 0.29)' nrd='0.29 / W' nrs='0.29 / W'
+ sa=0 sb=0 sd=0 mult=1 m=1
XM60 net2 Vp net3 VDD sky130_fd_pr__pfet_g5v0d10v5 L=0.5 W=4 nf=2 ad='int((nf+1)/2) * W/nf * 0.29' as='int((nf+2)/2) * W/nf * 0.29'
+ pd='2*int((nf+1)/2) * (W/nf + 0.29)' ps='2*int((nf+2)/2) * (W/nf + 0.29)' nrd='0.29 / W' nrs='0.29 / W'
+ sa=0 sb=0 sd=0 mult=1 m=1
.ends


* expanding   symbol:  sky130_ak_ip__comparator/xschem/level_shifter_up.sym # of pins=7
** sym_path: xschem/level_shifter_up.sym
** sch_path: xschem/level_shifter_up.sch
.subckt level_shifter_up VDD_HV VDD_LV GND_LV xb_hv x_hv x_lv GND_HV
*.ipin VDD_HV
*.ipin GND_HV
*.ipin x_lv
*.ipin VDD_LV
*.opin x_hv
*.opin xb_hv
*.ipin GND_LV
XM65 xb_hv x_lv GND_HV GND_HV sky130_fd_pr__nfet_g5v0d10v5 L=0.5 W=1 nf=1 ad='int((nf+1)/2) * W/nf * 0.29'
+ as='int((nf+2)/2) * W/nf * 0.29' pd='2*int((nf+1)/2) * (W/nf + 0.29)' ps='2*int((nf+2)/2) * (W/nf + 0.29)'
+ nrd='0.29 / W' nrs='0.29 / W' sa=0 sb=0 sd=0 mult=1 m=1
XM66 x_hv xb_lv GND_HV GND_HV sky130_fd_pr__nfet_g5v0d10v5 L=0.5 W=1 nf=1 ad='int((nf+1)/2) * W/nf * 0.29'
+ as='int((nf+2)/2) * W/nf * 0.29' pd='2*int((nf+1)/2) * (W/nf + 0.29)' ps='2*int((nf+2)/2) * (W/nf + 0.29)'
+ nrd='0.29 / W' nrs='0.29 / W' sa=0 sb=0 sd=0 mult=1 m=1
XM67 xb_hv x_hv VDD_HV VDD_HV sky130_fd_pr__pfet_g5v0d10v5 L=0.5 W=0.5 nf=1 ad='int((nf+1)/2) * W/nf * 0.29'
+ as='int((nf+2)/2) * W/nf * 0.29' pd='2*int((nf+1)/2) * (W/nf + 0.29)' ps='2*int((nf+2)/2) * (W/nf + 0.29)'
+ nrd='0.29 / W' nrs='0.29 / W' sa=0 sb=0 sd=0 mult=1 m=1
XM68 x_hv xb_hv VDD_HV VDD_HV sky130_fd_pr__pfet_g5v0d10v5 L=0.5 W=0.5 nf=1 ad='int((nf+1)/2) * W/nf * 0.29'
+ as='int((nf+2)/2) * W/nf * 0.29' pd='2*int((nf+1)/2) * (W/nf + 0.29)' ps='2*int((nf+2)/2) * (W/nf + 0.29)'
+ nrd='0.29 / W' nrs='0.29 / W' sa=0 sb=0 sd=0 mult=1 m=1
x1 VDD_LV xb_lv x_lv GND_LV inverter
.ends


* expanding   symbol:  sky130_ak_ip__comparator/xschem/inverter.sym # of pins=4
** sym_path: xschem/inverter.sym
** sch_path: xschem/inverter.sch
.subckt inverter VDD xb x GND
*.ipin VDD
*.ipin GND
*.opin xb
*.ipin x
XM31 xb x VDD VDD sky130_fd_pr__pfet_01v8 L=1 W=2 nf=1 ad='int((nf+1)/2) * W/nf * 0.29' as='int((nf+2)/2) * W/nf * 0.29'
+ pd='2*int((nf+1)/2) * (W/nf + 0.29)' ps='2*int((nf+2)/2) * (W/nf + 0.29)' nrd='0.29 / W' nrs='0.29 / W'
+ sa=0 sb=0 sd=0 mult=1 m=1
XM44 xb x GND GND sky130_fd_pr__nfet_01v8 L=1 W=1 nf=1 ad='int((nf+1)/2) * W/nf * 0.29' as='int((nf+2)/2) * W/nf * 0.29'
+ pd='2*int((nf+1)/2) * (W/nf + 0.29)' ps='2*int((nf+2)/2) * (W/nf + 0.29)' nrd='0.29 / W' nrs='0.29 / W'
+ sa=0 sb=0 sd=0 mult=1 m=1
.ends

.GLOBAL GND
.end
